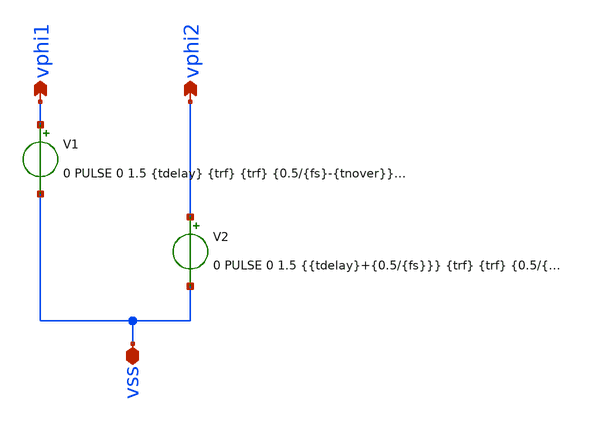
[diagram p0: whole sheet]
** sch_path: xschem/clk_noverlap_ideal.sch
**.subckt clk_noverlap_ideal vss vphi1 vphi2
*.iopin vss
*.opin vphi1
*.opin vphi2
V1 vphi1 vss 0 PULSE 0 1.5 {tdelay} {trf} {trf} {0.5/{fs}-{tnover}} {1/{fs}} 0
V2 vphi2 vss 0 PULSE 0 1.5 {{tdelay}+{0.5/{fs}}} {trf} {trf} {0.5/{fs}-{tnover}} {1/{fs}} 0
**.ends
.end
